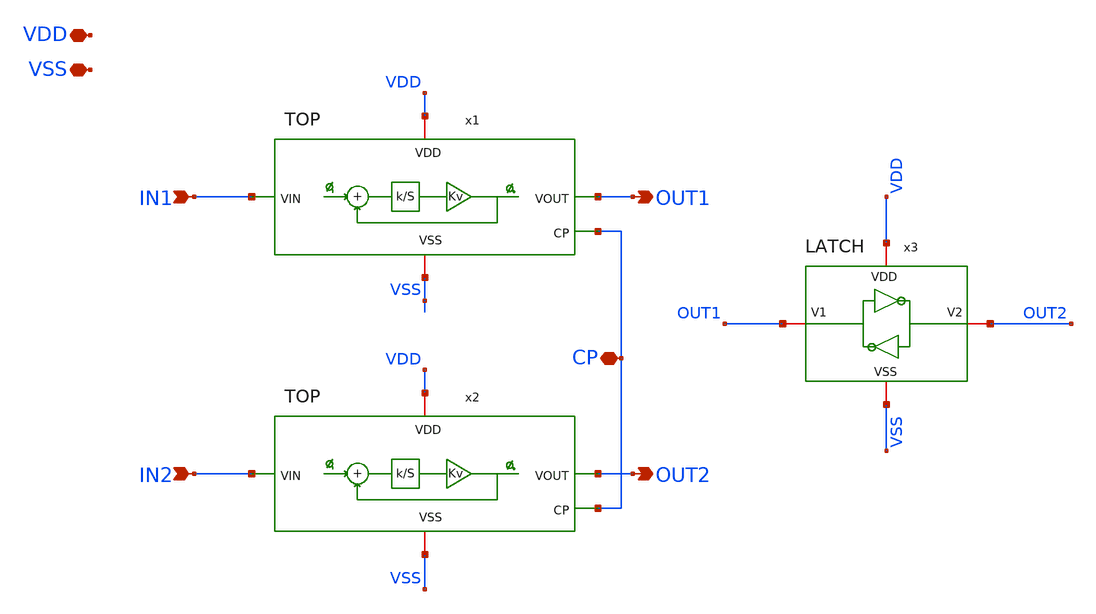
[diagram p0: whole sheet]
** sch_path: xschem/Cells/QDLL_TOP.sch
**.subckt QDLL_TOP VDD VSS IN1 IN2 OUT1 OUT2 CP
*.iopin VDD
*.iopin VSS
*.ipin IN1
*.ipin IN2
*.opin OUT1
*.opin OUT2
*.iopin CP
x1 VDD OUT1 IN1 VSS CP TOP
x2 VDD OUT2 IN2 VSS CP TOP
x3 VSS OUT1 VDD OUT2 LATCH
**.ends
.end
